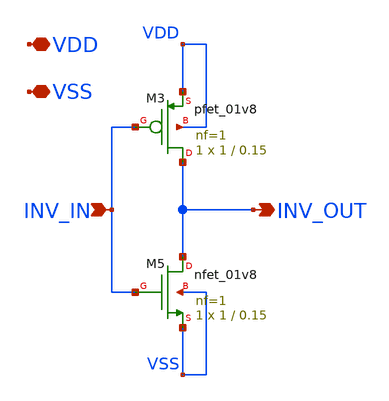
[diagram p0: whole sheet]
** sch_path: xschem/inv_x1.sch
**.subckt inv_x1 INV_IN INV_OUT VDD VSS
*.ipin INV_IN
*.opin INV_OUT
*.iopin VDD
*.iopin VSS
XM3 INV_OUT INV_IN VDD VDD sky130_fd_pr__pfet_01v8 L=0.15 W=1 nf=1 ad='int((nf+1)/2) * W/nf * 0.29' as='int((nf+2)/2) * W/nf * 0.29'
+ pd='2*int((nf+1)/2) * (W/nf + 0.29)' ps='2*int((nf+2)/2) * (W/nf + 0.29)' nrd='0.29 / W' nrs='0.29 / W'
+ sa=0 sb=0 sd=0 mult=1 m=1
XM5 INV_OUT INV_IN VSS VSS sky130_fd_pr__nfet_01v8 L=0.15 W=1 nf=1 ad='int((nf+1)/2) * W/nf * 0.29' as='int((nf+2)/2) * W/nf * 0.29'
+ pd='2*int((nf+1)/2) * (W/nf + 0.29)' ps='2*int((nf+2)/2) * (W/nf + 0.29)' nrd='0.29 / W' nrs='0.29 / W'
+ sa=0 sb=0 sd=0 mult=1 m=1
**.ends
.end
